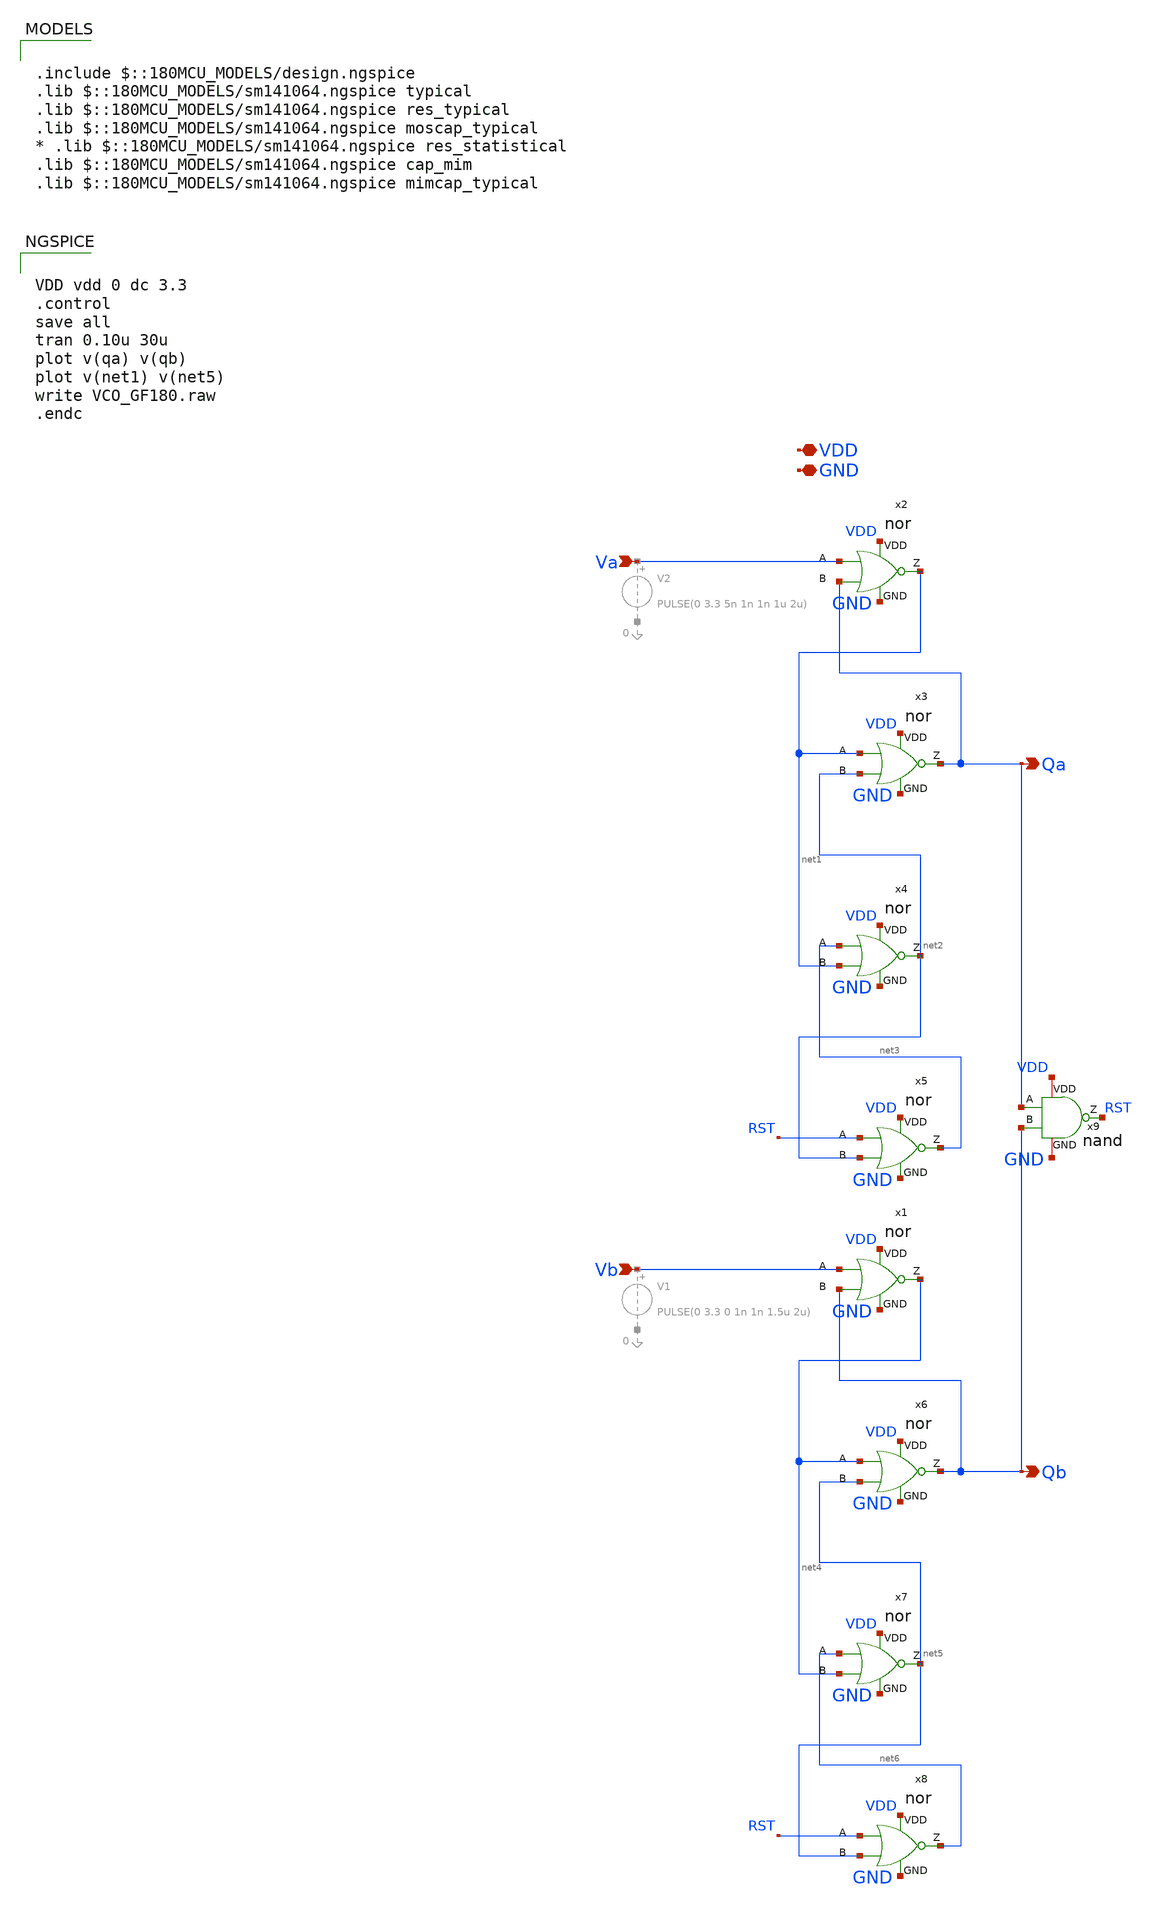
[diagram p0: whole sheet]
** sch_path: blocks/pll/pfd.sch
**.subckt pfd Vb Va Qa Qb VDD GND
*.ipin Vb
*.ipin Va
*.opin Qa
*.opin Qb
*.iopin VDD
*.iopin GND
x2 VDD Va Qa net1 GND nor
x3 VDD net1 net2 Qa GND nor
x4 VDD net3 net1 net2 GND nor
x5 VDD RST net2 net3 GND nor
x1 VDD Vb Qb net4 GND nor
x6 VDD net4 net5 Qb GND nor
x7 VDD net6 net4 net5 GND nor
x8 VDD RST net5 net6 GND nor
x9 VDD RST Qa Qb GND nand
**** begin user architecture code

.include $::180MCU_MODELS/design.ngspice
.lib $::180MCU_MODELS/sm141064.ngspice typical
.lib $::180MCU_MODELS/sm141064.ngspice res_typical
.lib $::180MCU_MODELS/sm141064.ngspice moscap_typical
* .lib $::180MCU_MODELS/sm141064.ngspice res_statistical
.lib $::180MCU_MODELS/sm141064.ngspice cap_mim
.lib $::180MCU_MODELS/sm141064.ngspice mimcap_typical



VDD vdd 0 dc 3.3
.control
save all
tran 0.10u 30u
plot v(qa) v(qb)
plot v(net1) v(net5)
write VCO_GF180.raw
.endc


**** end user architecture code
**.ends

* expanding   symbol:  blocks/pll/nor.sym # of pins=5
** sym_path: blocks/pll/nor.sym
** sch_path: blocks/pll/nor.sch
.subckt nor VDD A B Z GND
*.ipin A
*.ipin B
*.opin Z
*.iopin GND
*.iopin VDD
XM1 Z A GND GND nfet_03v3 L=0.28u W=0.22u nf=1 ad='int((nf+1)/2) * W/nf * 0.18u' as='int((nf+2)/2) * W/nf * 0.18u'
+ pd='2*int((nf+1)/2) * (W/nf + 0.18u)' ps='2*int((nf+2)/2) * (W/nf + 0.18u)' nrd='0.18u / W' nrs='0.18u / W'
+ sa=0 sb=0 sd=0 m=1
XM2 Z B net1 VDD pfet_03v3 L=0.28u W=0.22u nf=1 ad='int((nf+1)/2) * W/nf * 0.18u' as='int((nf+2)/2) * W/nf * 0.18u'
+ pd='2*int((nf+1)/2) * (W/nf + 0.18u)' ps='2*int((nf+2)/2) * (W/nf + 0.18u)' nrd='0.18u / W' nrs='0.18u / W'
+ sa=0 sb=0 sd=0 m=1
XM3 Z B GND GND nfet_03v3 L=0.28u W=0.22u nf=1 ad='int((nf+1)/2) * W/nf * 0.18u' as='int((nf+2)/2) * W/nf * 0.18u'
+ pd='2*int((nf+1)/2) * (W/nf + 0.18u)' ps='2*int((nf+2)/2) * (W/nf + 0.18u)' nrd='0.18u / W' nrs='0.18u / W'
+ sa=0 sb=0 sd=0 m=1
XM4 net1 A VDD VDD pfet_03v3 L=0.28u W=0.22u nf=1 ad='int((nf+1)/2) * W/nf * 0.18u' as='int((nf+2)/2) * W/nf * 0.18u'
+ pd='2*int((nf+1)/2) * (W/nf + 0.18u)' ps='2*int((nf+2)/2) * (W/nf + 0.18u)' nrd='0.18u / W' nrs='0.18u / W'
+ sa=0 sb=0 sd=0 m=1
.ends


* expanding   symbol:  blocks/pll/nand.sym # of pins=5
** sym_path: pll_block_templates_v1/layout2/nand.sym
** sch_path: pll_block_templates_v1/layout2/nand.sch
.subckt nand VDD Z A B GND
*.ipin A
*.iopin VDD
*.opin Z
*.iopin GND
*.ipin B
XM1 Z A net1 GND nfet_03v3 L=0.28u W=0.3u nf=1 ad='int((nf+1)/2) * W/nf * 0.18u' as='int((nf+2)/2) * W/nf * 0.18u'
+ pd='2*int((nf+1)/2) * (W/nf + 0.18u)' ps='2*int((nf+2)/2) * (W/nf + 0.18u)' nrd='0.18u / W' nrs='0.18u / W'
+ sa=0 sb=0 sd=0 m=1
XM2 Z A VDD VDD pfet_03v3 L=0.28u W=0.3u nf=1 ad='int((nf+1)/2) * W/nf * 0.18u' as='int((nf+2)/2) * W/nf * 0.18u'
+ pd='2*int((nf+1)/2) * (W/nf + 0.18u)' ps='2*int((nf+2)/2) * (W/nf + 0.18u)' nrd='0.18u / W' nrs='0.18u / W'
+ sa=0 sb=0 sd=0 m=1
XM3 Z B VDD VDD pfet_03v3 L=0.28u W=0.3u nf=1 ad='int((nf+1)/2) * W/nf * 0.18u' as='int((nf+2)/2) * W/nf * 0.18u'
+ pd='2*int((nf+1)/2) * (W/nf + 0.18u)' ps='2*int((nf+2)/2) * (W/nf + 0.18u)' nrd='0.18u / W' nrs='0.18u / W'
+ sa=0 sb=0 sd=0 m=1
XM4 net1 B GND GND nfet_03v3 L=0.28u W=0.3u nf=1 ad='int((nf+1)/2) * W/nf * 0.18u' as='int((nf+2)/2) * W/nf * 0.18u'
+ pd='2*int((nf+1)/2) * (W/nf + 0.18u)' ps='2*int((nf+2)/2) * (W/nf + 0.18u)' nrd='0.18u / W' nrs='0.18u / W'
+ sa=0 sb=0 sd=0 m=1
.ends

.end
